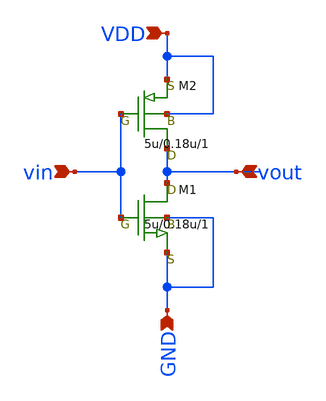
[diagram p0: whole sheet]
** sch_path: member_project/radioheadozawa/inverter/inverter.sch
**.subckt inverter VDD vin vout GND
*.ipin VDD
*.ipin vin
*.ipin vout
*.ipin GND
M1 vout vin GND GND nch w=5u l=0.18u as=0 ps=0 ad=0 pd=0 m=1
M2 vout vin VDD VDD pch w=5u l=0.18u as=0 ps=0 ad=0 pd=0 m=1
**.ends
.end
